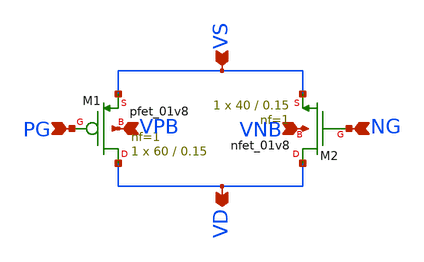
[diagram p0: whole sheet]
** sch_path: compiled 2/a_mux_switch.sch
**.subckt a_mux_switch PG NG VS VD VPB VNB
*.ipin PG
*.ipin NG
*.ipin VS
*.opin VD
*.ipin VPB
*.ipin VNB
XM1 VD PG VS VPB sky130_fd_pr__pfet_01v8 L=0.15 W=60 nf=1 ad='int((nf+1)/2) * W/nf * 0.29' as='int((nf+2)/2) * W/nf * 0.29'
+ pd='2*int((nf+1)/2) * (W/nf + 0.29)' ps='2*int((nf+2)/2) * (W/nf + 0.29)' nrd='0.29 / W' nrs='0.29 / W'
+ sa=0 sb=0 sd=0 mult=1 m=1
XM2 VD NG VS VNB sky130_fd_pr__nfet_01v8 L=0.15 W=40 nf=1 ad='int((nf+1)/2) * W/nf * 0.29' as='int((nf+2)/2) * W/nf * 0.29'
+ pd='2*int((nf+1)/2) * (W/nf + 0.29)' ps='2*int((nf+2)/2) * (W/nf + 0.29)' nrd='0.29 / W' nrs='0.29 / W'
+ sa=0 sb=0 sd=0 mult=1 m=1
**.ends
.end
